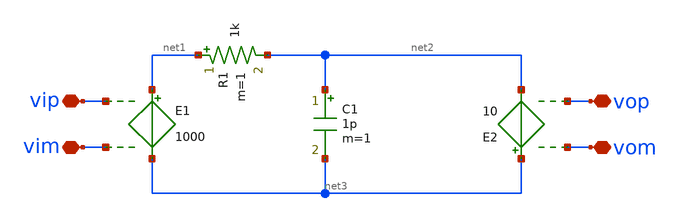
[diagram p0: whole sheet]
** sch_path: xschem/untitled-6.sch
**.subckt untitled-6 vip vim vop vom
*.iopin vip
*.iopin vim
*.iopin vop
*.iopin vom
E1 net1 net3 vip vim 1000
E2 net3 net2 vom vop 10
C1 net2 net3 1p m=1
R1 net1 net2 1k m=1
**.ends
.end
